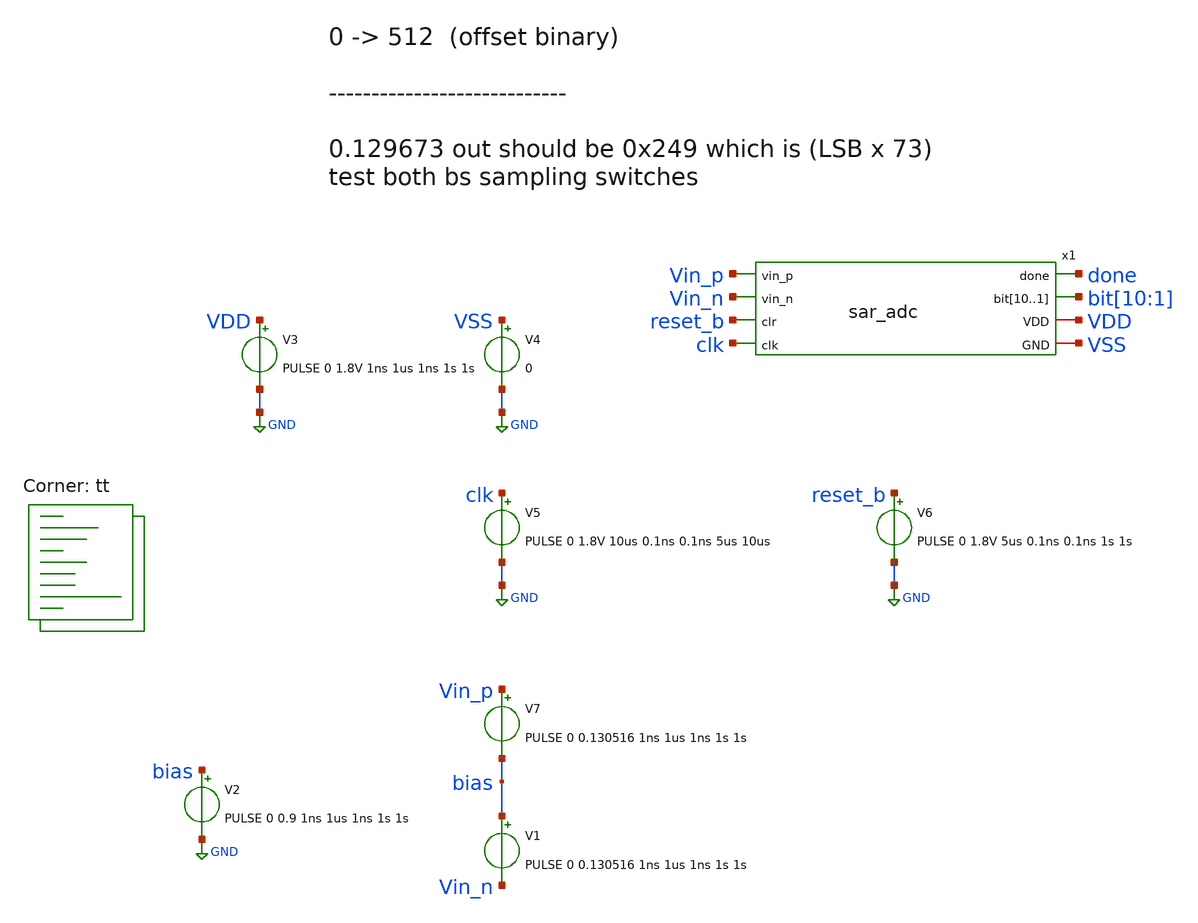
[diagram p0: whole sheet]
** sch_path: xschem/sar_adc/adc_test.sch
**.subckt adc_test
x1 done Vin_p bit[10] bit[9] bit[8] bit[7] bit[6] bit[5] bit[4] bit[3] bit[2] bit[1] Vin_n reset_b
+ VDD clk VSS sar_adc
V3 VDD GND PULSE 0 1.8V 1ns 1us 1ns 1s 1s
V4 VSS GND 0
V5 clk GND PULSE 0 1.8V 10us 0.1ns 0.1ns 5us 10us
V7 Vin_p bias PULSE 0 0.130516 1ns 1us 1ns 1s 1s
V1 bias Vin_n PULSE 0 0.130516 1ns 1us 1ns 1s 1s
V6 reset_b GND PULSE 0 1.8V 5us 0.1ns 0.1ns 1s 1s
V2 bias GND PULSE 0 0.9 1ns 1us 1ns 1s 1s
**** begin user architecture code
.lib $::SKYWATER_MODELS/sky130.lib.spice tt

*.lib $::SKYWATER_MODELS/sky130.lib.spice tt

* .lib $::SKYWATER_MODELS/sky130.lib.spice.tt.red tt

.include $::SKYWATER_STDCELLS/sky130_fd_sc_hd.spice




.control
tran 0.1u 340u uic

write adc_test.raw
.endc




**** end user architecture code
**.ends
.GLOBAL GND
.end
